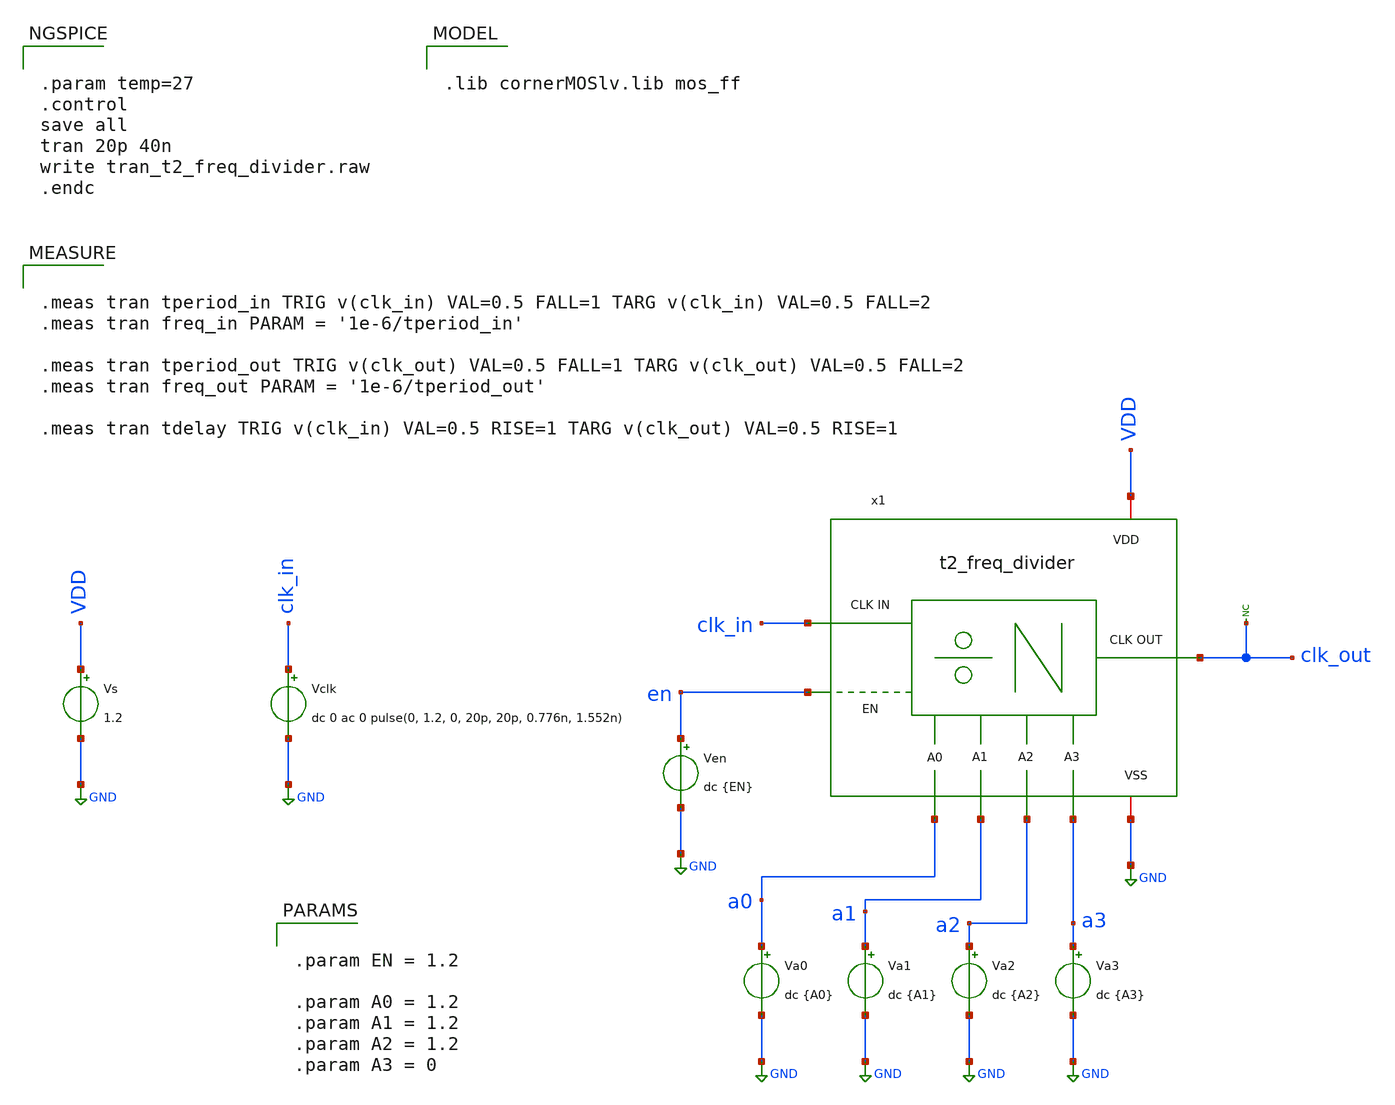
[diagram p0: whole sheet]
** sch_path: Team 2 Design/design_data/xschem/t2_freq_divider_tb.sch
**.subckt t2_freq_divider_tb
Vs VDD GND 1.2
Vclk clk_in GND dc 0 ac 0 pulse(0, 1.2, 0, 20p, 20p, 0.776n, 1.552n)
x1 VDD GND clk_in en a0 a1 a2 a3 clk_out t2_freq_divider
* noconn clk_out
Ven en GND dc {EN}
Va0 a0 GND dc {A0}
Va1 a1 GND dc {A1}
Va2 a2 GND dc {A2}
Va3 a3 GND dc {A3}
**** begin user architecture code


.param temp=27
.control
save all
tran 20p 40n
write tran_t2_freq_divider.raw
.endc



.lib cornerMOSlv.lib mos_ff



.meas tran tperiod_in TRIG v(clk_in) VAL=0.5 FALL=1 TARG v(clk_in) VAL=0.5 FALL=2
.meas tran freq_in PARAM = '1e-6/tperiod_in'

.meas tran tperiod_out TRIG v(clk_out) VAL=0.5 FALL=1 TARG v(clk_out) VAL=0.5 FALL=2
.meas tran freq_out PARAM = '1e-6/tperiod_out'

.meas tran tdelay TRIG v(clk_in) VAL=0.5 RISE=1 TARG v(clk_out) VAL=0.5 RISE=1




.param EN = 1.2

.param A0 = 1.2
.param A1 = 1.2
.param A2 = 1.2
.param A3 = 0


**** end user architecture code
**.ends
.GLOBAL GND
.end
